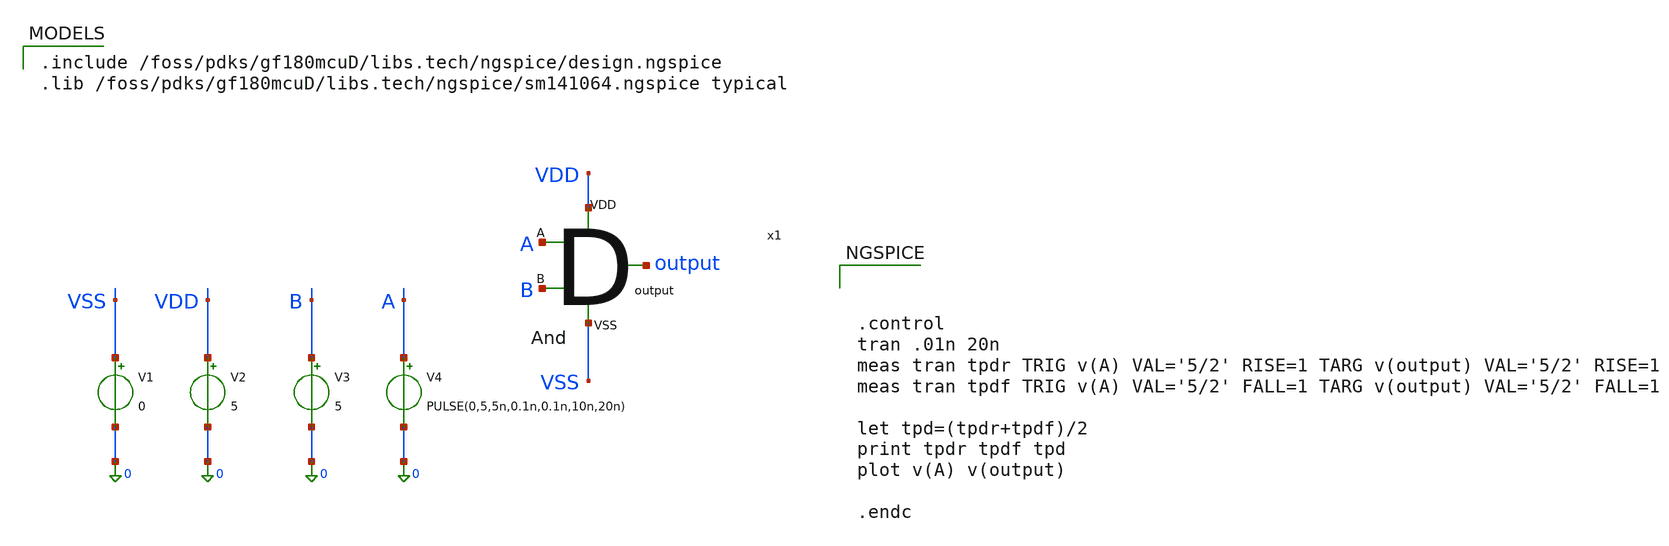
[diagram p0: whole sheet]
** sch_path: activities/opamp3AKAM/delayTB.sch
**.subckt delayTB
x1 A VDD B output VSS andGate
V1 VSS 0 0
V2 VDD 0 5
V3 B 0 5
V4 A 0 PULSE(0,5,5n,0.1n,0.1n,10n,20n)
**** begin user architecture code

.include /foss/pdks/gf180mcuD/libs.tech/ngspice/design.ngspice
.lib /foss/pdks/gf180mcuD/libs.tech/ngspice/sm141064.ngspice typical




.control
tran .01n 20n
meas tran tpdr TRIG v(A) VAL='5/2' RISE=1 TARG v(output) VAL='5/2' RISE=1
meas tran tpdf TRIG v(A) VAL='5/2' FALL=1 TARG v(output) VAL='5/2' FALL=1

let tpd=(tpdr+tpdf)/2
print tpdr tpdf tpd
plot v(A) v(output)

.endc


**** end user architecture code
**.ends
.end
